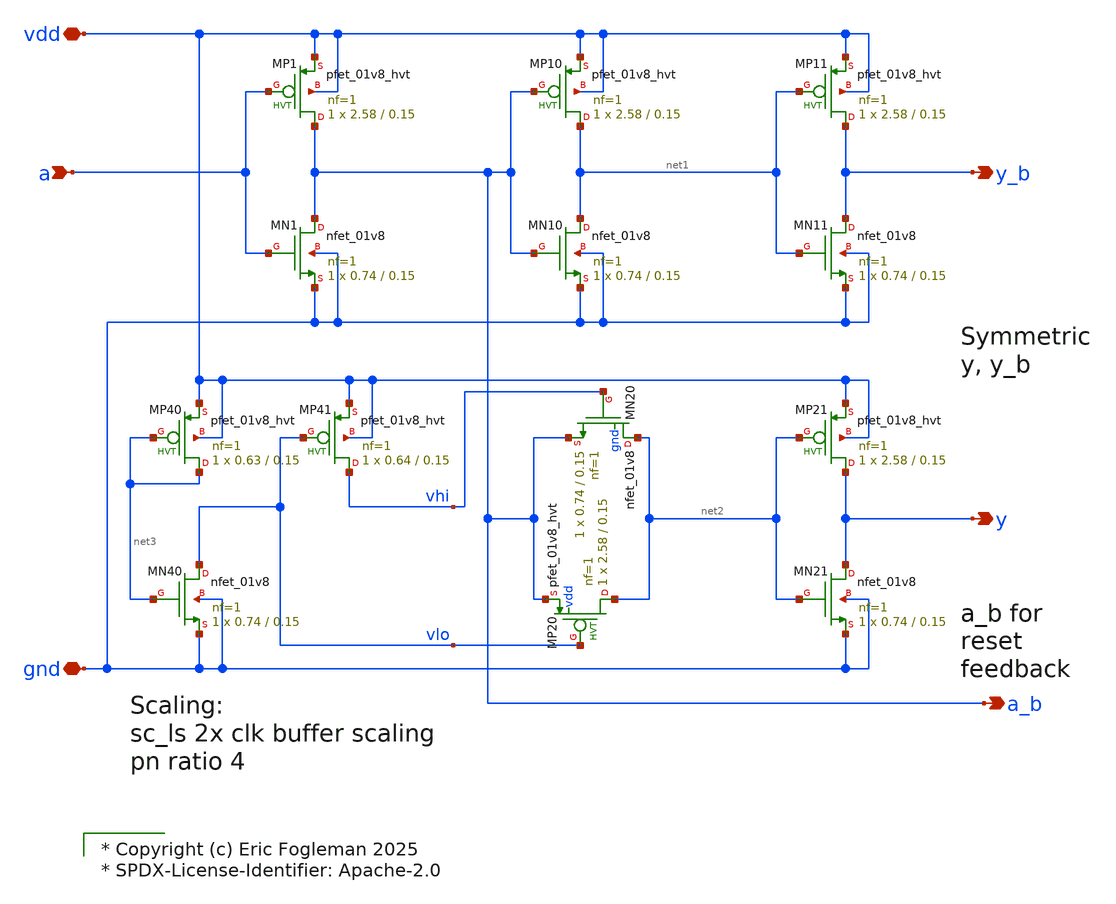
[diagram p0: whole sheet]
** sch_path: xschem/ejf_pll96_diff_buf.sch

* Copyright (c) Eric Fogleman 2025
* SPDX-License-Identifier: Apache-2.0

**.subckt ejf_pll96_diff_buf vdd gnd a y_b y a_b
*.iopin vdd
*.iopin gnd
*.ipin a
*.opin y_b
*.opin y
*.opin a_b
XMN1 a_b a gnd gnd sky130_fd_pr__nfet_01v8 L=0.15 W=0.74 nf=1 ad='int((nf+1)/2) * W/nf * 0.29' as='int((nf+2)/2) * W/nf * 0.29'
+ pd='2*int((nf+1)/2) * (W/nf + 0.29)' ps='2*int((nf+2)/2) * (W/nf + 0.29)' nrd='0.29 / W' nrs='0.29 / W'
+ sa=0 sb=0 sd=0 mult=1 m=1
XMP1 a_b a vdd vdd sky130_fd_pr__pfet_01v8_hvt L=0.15 W=2.58 nf=1 ad='int((nf+1)/2) * W/nf * 0.29' as='int((nf+2)/2) * W/nf * 0.29'
+ pd='2*int((nf+1)/2) * (W/nf + 0.29)' ps='2*int((nf+2)/2) * (W/nf + 0.29)' nrd='0.29 / W' nrs='0.29 / W'
+ sa=0 sb=0 sd=0 mult=1 m=1
XMN11 y_b net1 gnd gnd sky130_fd_pr__nfet_01v8 L=0.15 W=0.74 nf=1 ad='int((nf+1)/2) * W/nf * 0.29' as='int((nf+2)/2) * W/nf * 0.29'
+ pd='2*int((nf+1)/2) * (W/nf + 0.29)' ps='2*int((nf+2)/2) * (W/nf + 0.29)' nrd='0.29 / W' nrs='0.29 / W'
+ sa=0 sb=0 sd=0 mult=1 m=1
XMP11 y_b net1 vdd vdd sky130_fd_pr__pfet_01v8_hvt L=0.15 W=2.58 nf=1 ad='int((nf+1)/2) * W/nf * 0.29'
+ as='int((nf+2)/2) * W/nf * 0.29' pd='2*int((nf+1)/2) * (W/nf + 0.29)' ps='2*int((nf+2)/2) * (W/nf + 0.29)'
+ nrd='0.29 / W' nrs='0.29 / W' sa=0 sb=0 sd=0 mult=1 m=1
XMN10 net1 a_b gnd gnd sky130_fd_pr__nfet_01v8 L=0.15 W=0.74 nf=1 ad='int((nf+1)/2) * W/nf * 0.29' as='int((nf+2)/2) * W/nf * 0.29'
+ pd='2*int((nf+1)/2) * (W/nf + 0.29)' ps='2*int((nf+2)/2) * (W/nf + 0.29)' nrd='0.29 / W' nrs='0.29 / W'
+ sa=0 sb=0 sd=0 mult=1 m=1
XMP10 net1 a_b vdd vdd sky130_fd_pr__pfet_01v8_hvt L=0.15 W=2.58 nf=1 ad='int((nf+1)/2) * W/nf * 0.29'
+ as='int((nf+2)/2) * W/nf * 0.29' pd='2*int((nf+1)/2) * (W/nf + 0.29)' ps='2*int((nf+2)/2) * (W/nf + 0.29)'
+ nrd='0.29 / W' nrs='0.29 / W' sa=0 sb=0 sd=0 mult=1 m=1
XMN21 y net2 gnd gnd sky130_fd_pr__nfet_01v8 L=0.15 W=0.74 nf=1 ad='int((nf+1)/2) * W/nf * 0.29' as='int((nf+2)/2) * W/nf * 0.29'
+ pd='2*int((nf+1)/2) * (W/nf + 0.29)' ps='2*int((nf+2)/2) * (W/nf + 0.29)' nrd='0.29 / W' nrs='0.29 / W'
+ sa=0 sb=0 sd=0 mult=1 m=1
XMP21 y net2 vdd vdd sky130_fd_pr__pfet_01v8_hvt L=0.15 W=2.58 nf=1 ad='int((nf+1)/2) * W/nf * 0.29'
+ as='int((nf+2)/2) * W/nf * 0.29' pd='2*int((nf+1)/2) * (W/nf + 0.29)' ps='2*int((nf+2)/2) * (W/nf + 0.29)'
+ nrd='0.29 / W' nrs='0.29 / W' sa=0 sb=0 sd=0 mult=1 m=1
XMP20 net2 vlo a_b vdd sky130_fd_pr__pfet_01v8_hvt L=0.15 W=2.58 nf=1 ad='int((nf+1)/2) * W/nf * 0.29'
+ as='int((nf+2)/2) * W/nf * 0.29' pd='2*int((nf+1)/2) * (W/nf + 0.29)' ps='2*int((nf+2)/2) * (W/nf + 0.29)'
+ nrd='0.29 / W' nrs='0.29 / W' sa=0 sb=0 sd=0 mult=1 m=1
XMN20 net2 vhi a_b gnd sky130_fd_pr__nfet_01v8 L=0.15 W=0.74 nf=1 ad='int((nf+1)/2) * W/nf * 0.29' as='int((nf+2)/2) * W/nf * 0.29'
+ pd='2*int((nf+1)/2) * (W/nf + 0.29)' ps='2*int((nf+2)/2) * (W/nf + 0.29)' nrd='0.29 / W' nrs='0.29 / W'
+ sa=0 sb=0 sd=0 mult=1 m=1
XMN40 vlo net3 gnd gnd sky130_fd_pr__nfet_01v8 L=0.15 W=0.74 nf=1 ad='int((nf+1)/2) * W/nf * 0.29' as='int((nf+2)/2) * W/nf * 0.29'
+ pd='2*int((nf+1)/2) * (W/nf + 0.29)' ps='2*int((nf+2)/2) * (W/nf + 0.29)' nrd='0.29 / W' nrs='0.29 / W'
+ sa=0 sb=0 sd=0 mult=1 m=1
XMP40 net3 net3 vdd vdd sky130_fd_pr__pfet_01v8_hvt L=0.15 W=0.63 nf=1 ad='int((nf+1)/2) * W/nf * 0.29'
+ as='int((nf+2)/2) * W/nf * 0.29' pd='2*int((nf+1)/2) * (W/nf + 0.29)' ps='2*int((nf+2)/2) * (W/nf + 0.29)'
+ nrd='0.29 / W' nrs='0.29 / W' sa=0 sb=0 sd=0 mult=1 m=1
XMP41 vhi vlo vdd vdd sky130_fd_pr__pfet_01v8_hvt L=0.15 W=0.64 nf=1 ad='int((nf+1)/2) * W/nf * 0.29'
+ as='int((nf+2)/2) * W/nf * 0.29' pd='2*int((nf+1)/2) * (W/nf + 0.29)' ps='2*int((nf+2)/2) * (W/nf + 0.29)'
+ nrd='0.29 / W' nrs='0.29 / W' sa=0 sb=0 sd=0 mult=1 m=1
**.ends
.end
